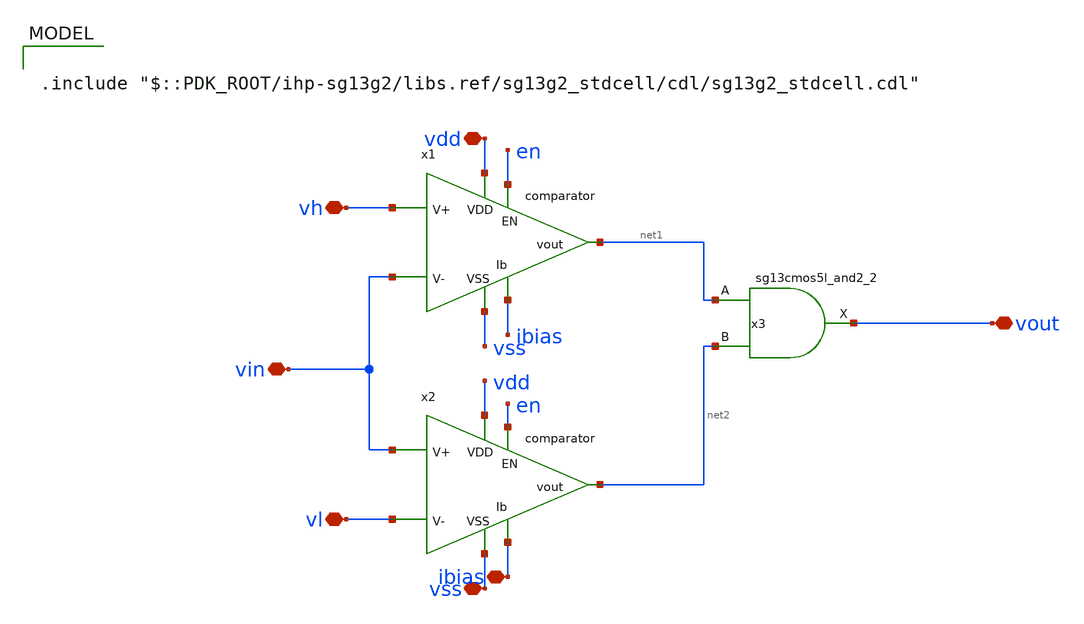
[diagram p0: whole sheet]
** sch_path: schematic/xschem/wind_comp/wind_comp.sch

.include "$::PDK_ROOT/ihp-sg13g2/libs.ref/sg13g2_stdcell/cdl/sg13g2_stdcell.cdl"

**.subckt wind_comp vdd vout vl vh ibias vss vin
*.iopin vdd
*.iopin vout
*.iopin vl
*.iopin vh
*.iopin ibias
*.iopin vss
*.iopin vin
x1 vdd net1 vh vin ibias vss en comparator
x2 vdd net2 vin vl ibias vss en comparator
x3 vout net1 net2 VDD VSS sg13g2_and2_2
**.ends

* expanding   symbol:
*+  /foss/designs/ic_design/chipaloza/sg13cmos5l_Wind_Comp/schematic/xschem/comparator/comparator.sym # of pins=7
** sym_path: schematic/xschem/comparator/comparator.sym
** sch_path: schematic/xschem/comparator/comparator.sch
.subckt comparator vdd vout v- v+ ibias vss en
*.iopin vdd
*.iopin vss
*.iopin v-
*.iopin v+
*.iopin ibias
*.iopin vout
*.iopin en
XM6 votap v+ tail vss sg13_lv_nmos w=0.26u l=3u ng=1 m=2 mm_ok=1
XM8 vdd votap votap vdd sg13_lv_pmos w=0.35u l=1u ng=1 m=2 mm_ok=1
XM9 votan v- tail vss sg13_lv_nmos w=0.26u l=3u ng=1 m=2 mm_ok=1
XM10 vdd votan votan vdd sg13_lv_pmos w=0.35u l=1u ng=1 m=2 mm_ok=1
XM11 tail ibias_en vss vss sg13_lv_nmos w=5u l=3u ng=1 m=4 mm_ok=1
x1 vdd votan vom vop vss vss decision_circuit
x2 vdd votap vop vom vss vss decision_circuit
x3 net2 net1 VDD VSS sg13g2_inv_16
x4 vdd ibias_en vop vom net1 vss en_n en final_stage_ota
x5 vout net2 VDD VSS sg13g2_inv_16
XM12 ibias_en ibias_en vss vss sg13_lv_nmos w=5u l=3u ng=1 m=2 mm_ok=1
XMB1 vdd en votap vdd sg13_lv_pmos w=0.15u l=0.13u ng=1 m=1 mm_ok=1
XMB2 vdd en votan vdd sg13_lv_pmos w=0.15u l=0.13u ng=1 m=1 mm_ok=1
XMB5 vss en_n ibias_en vss sg13_lv_nmos w=0.15u l=0.13u ng=1 m=1 mm_ok=1
x6 en_n en vdd vss sg13g2_inv_1
XMB3 ibias_en en ibias vss sg13_lv_nmos w=0.15u l=0.13u ng=1 m=3 mm_ok=1
x7 en VDD VSS sg13g2_antennanp
XM1 vss vss votan vss sg13_lv_nmos w=0.26u l=0.5u ng=1 m=2 mm_ok=1
XM2 vss vss votap vss sg13_lv_nmos w=0.26u l=0.5u ng=1 m=2 mm_ok=1
XM3 vss vss ibias_en vss sg13_lv_nmos w=5u l=0.5u ng=1 m=2 mm_ok=1
XM5 vss vss vss vss sg13_lv_nmos w=63.72u l=0.5u ng=20 m=1 mm_ok=1
XM4 vdd vdd vdd vdd sg13_lv_pmos w=17.88u l=0.5u ng=20 m=1 mm_ok=1
.ends


* expanding   symbol:
*+  /foss/designs/ic_design/chipaloza/sg13cmos5l_Wind_Comp/schematic/xschem/decision_circuit/decision_circuit.sym # of pins=6
** sym_path: schematic/xschem/decision_circuit/decision_circuit.sym
** sch_path: schematic/xschem/decision_circuit/decision_circuit.sch
.subckt decision_circuit vdd vota vout vota_n vss shift
*.iopin vota
*.iopin shift
*.iopin vota_n
*.iopin vdd
*.iopin vss
*.iopin vout
XM1 vout vota vdd vdd sg13_lv_pmos w=0.7u l=1u ng=1 m=1 mm_ok=1
XM2 vout vout shift vss sg13_lv_nmos w=0.26u l=10u ng=1 m=2 mm_ok=1
XM3 vout vota_n shift vss sg13_lv_nmos w=0.26u l=10u ng=1 m=2 mm_ok=1
XM4 vss vss vout vss sg13_lv_nmos w=0.26u l=0.5u ng=1 m=4 mm_ok=1
XM5 vdd vdd vout vdd sg13_lv_pmos w=0.35u l=0.5u ng=1 m=2 mm_ok=1
.ends


* expanding   symbol:
*+  /foss/designs/ic_design/chipaloza/sg13cmos5l_Wind_Comp/schematic/xschem/final_stage_ota/final_stage_ota.sym # of pins=8
** sym_path: schematic/xschem/final_stage_ota/final_stage_ota.sym
** sch_path: schematic/xschem/final_stage_ota/final_stage_ota.sch
.subckt final_stage_ota vdd iout vop vom vout vss en_n en
*.iopin vdd
*.iopin vom
*.iopin vop
*.iopin vss
*.iopin vout
*.iopin iout
*.ipin en_n
*.ipin en
XM1 vdd ibp vt vdd sg13_lv_pmos w=1u l=3u ng=1 m=2 mm_ok=1
XM2 n_mrr n_mrr vss vss sg13_lv_nmos w=0.15u l=3u ng=1 m=2 mm_ok=1
XM3 vt vom n_mrr vdd sg13_lv_pmos w=3.12u l=1u ng=1 m=2 mm_ok=1
XM4 vout n_mrr vss vss sg13_lv_nmos w=0.15u l=3u ng=1 m=2 mm_ok=1
XM5 vt vop vout vdd sg13_lv_pmos w=3.12u l=1u ng=1 m=2 mm_ok=1
XM6 ibp iout vss vss sg13_lv_nmos w=5u l=3u ng=1 m=2 mm_ok=1
XM7 vdd ibp ibp vdd sg13_lv_pmos w=1u l=3u ng=1 m=1 mm_ok=1
XMB3 vss en_n n_mrr vss sg13_lv_nmos w=0.15u l=0.13u ng=1 m=1 mm_ok=1
XMB4 vdd en ibp vdd sg13_lv_pmos w=0.15u l=0.13u ng=1 m=1 mm_ok=1
XM8 vss vss n_mrr vss sg13_lv_nmos w=0.15u l=0.5u ng=1 m=2 mm_ok=1
XM9 vss vss vout vss sg13_lv_nmos w=0.15u l=0.5u ng=1 m=2 mm_ok=1
XM10 vss vss ibp vss sg13_lv_nmos w=5u l=0.5u ng=1 m=2 mm_ok=1
XM11 vdd vdd vt vdd sg13_lv_pmos w=0.5u l=0.5u ng=1 m=2 mm_ok=1
XM12 vdd vdd ibp vdd sg13_lv_pmos w=0.5u l=0.5u ng=1 m=2 mm_ok=1
XM13 vdd vdd vout vdd sg13_lv_pmos w=3.12u l=0.5u ng=1 m=2 mm_ok=1
XM14 vdd vdd n_mrr vdd sg13_lv_pmos w=3.12u l=0.5u ng=1 m=2 mm_ok=1
.ends

.end
